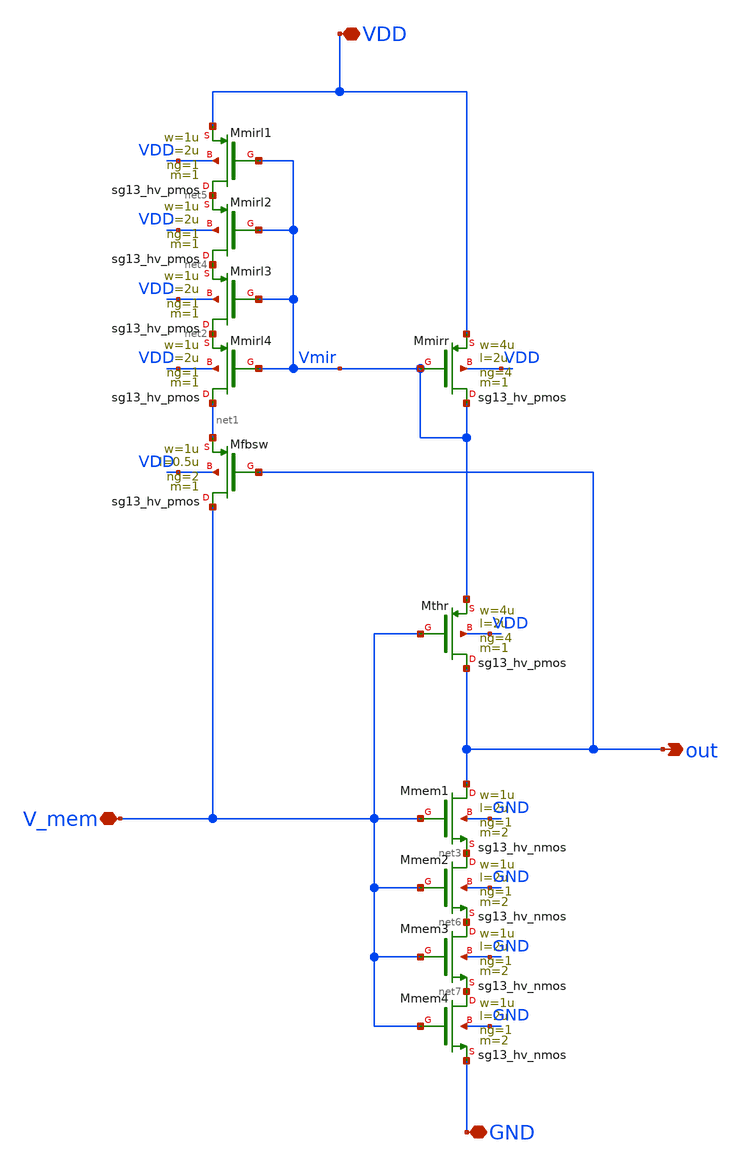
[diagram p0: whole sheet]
** sch_path: xschem/FB_system_bak.sch
**.subckt FB_system_bak out V_mem VDD GND
*.opin out
*.iopin V_mem
*.iopin VDD
*.iopin GND
XMmirr Vmir Vmir VDD VDD sg13_hv_pmos w=4u l=2u ng=4 m=1 mm_ok=1
XMfbsw V_mem out net1 VDD sg13_hv_pmos w=1u l=0.5u ng=2 m=1 mm_ok=1
XMmirl4 net1 Vmir net2 VDD sg13_hv_pmos w=1u l=2u ng=1 m=1 mm_ok=1
XMthr out V_mem Vmir VDD sg13_hv_pmos w=4u l=2u ng=4 m=1 mm_ok=1
XMmem1 out V_mem net3 GND sg13_hv_nmos w=1u l=2u ng=1 m=2 mm_ok=1
XMmirl3 net2 Vmir net4 VDD sg13_hv_pmos w=1u l=2u ng=1 m=1 mm_ok=1
XMmirl2 net4 Vmir net5 VDD sg13_hv_pmos w=1u l=2u ng=1 m=1 mm_ok=1
XMmirl1 net5 Vmir VDD VDD sg13_hv_pmos w=1u l=2u ng=1 m=1 mm_ok=1
XMmem2 net3 V_mem net6 GND sg13_hv_nmos w=1u l=2u ng=1 m=2 mm_ok=1
XMmem3 net6 V_mem net7 GND sg13_hv_nmos w=1u l=2u ng=1 m=2 mm_ok=1
XMmem4 net7 V_mem GND GND sg13_hv_nmos w=1u l=2u ng=1 m=2 mm_ok=1
**.ends
.end
